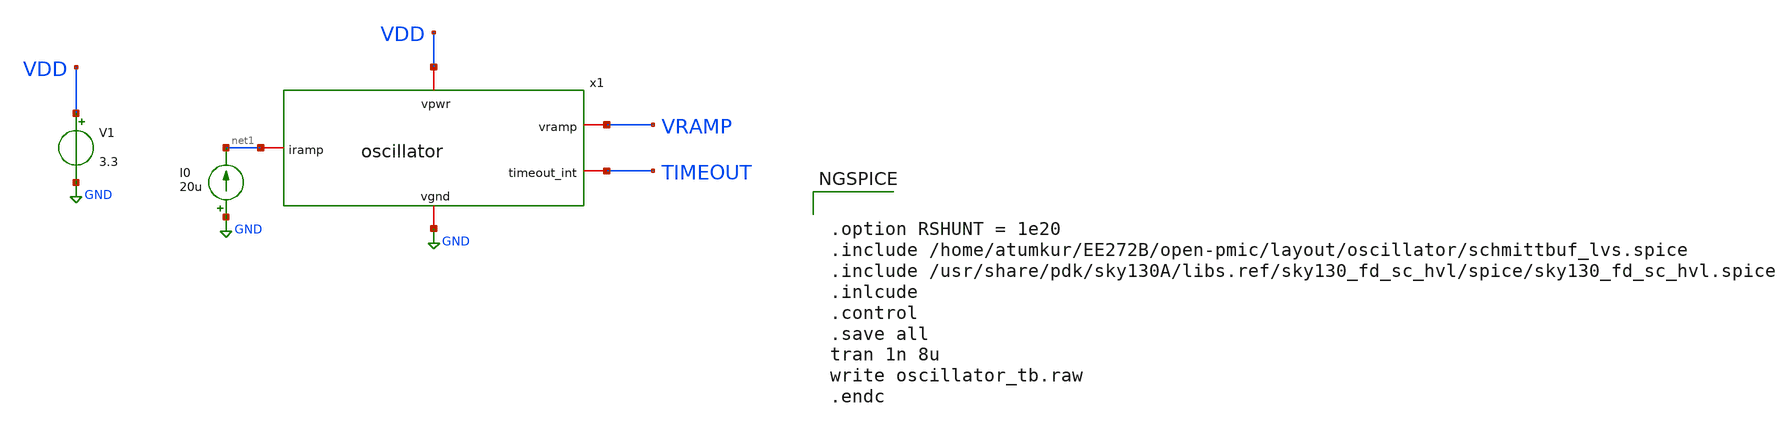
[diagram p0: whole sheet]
** sch_path: design/oscillator/oscillator_tb.sch
**.subckt oscillator_tb
x1 VDD GND net1 VRAMP TIMEOUT oscillator
V1 VDD GND 3.3
I0 GND net1 20u
**** begin user architecture code

.include $::SKYWATER_MODELS/cells/nfet_01v8/sky130_fd_pr__nfet_01v8__tt.corner.spice
.include $::SKYWATER_MODELS/cells/nfet_01v8_lvt/sky130_fd_pr__nfet_01v8_lvt__tt.corner.spice
.include $::SKYWATER_MODELS/cells/pfet_01v8/sky130_fd_pr__pfet_01v8__tt.corner.spice
.include $::SKYWATER_MODELS/cells/nfet_03v3_nvt/sky130_fd_pr__nfet_03v3_nvt__tt.corner.spice
.include $::SKYWATER_MODELS/cells/nfet_05v0_nvt/sky130_fd_pr__nfet_05v0_nvt__tt.corner.spice
.include $::SKYWATER_MODELS/cells/esd_nfet_01v8/sky130_fd_pr__esd_nfet_01v8__tt.corner.spice
.include $::SKYWATER_MODELS/cells/pfet_01v8_lvt/sky130_fd_pr__pfet_01v8_lvt__tt.corner.spice
.include $::SKYWATER_MODELS/cells/pfet_01v8_hvt/sky130_fd_pr__pfet_01v8_hvt__tt.corner.spice
.include $::SKYWATER_MODELS/cells/esd_pfet_g5v0d10v5/sky130_fd_pr__esd_pfet_g5v0d10v5__tt.corner.spice
.include $::SKYWATER_MODELS/cells/pfet_g5v0d10v5/sky130_fd_pr__pfet_g5v0d10v5__tt.corner.spice
.include $::SKYWATER_MODELS/cells/pfet_g5v0d16v0/sky130_fd_pr__pfet_g5v0d16v0__tt.corner.spice
.include $::SKYWATER_MODELS/cells/nfet_g5v0d10v5/sky130_fd_pr__nfet_g5v0d10v5__tt.corner.spice
.include $::SKYWATER_MODELS/cells/nfet_g5v0d16v0/sky130_fd_pr__nfet_g5v0d16v0__tt_discrete.corner.spice
.include $::SKYWATER_MODELS/cells/esd_nfet_g5v0d10v5/sky130_fd_pr__esd_nfet_g5v0d10v5__tt.corner.spice
.include $::SKYWATER_MODELS/models/corners/tt/nonfet.spice
* Mismatch parameters
.include $::SKYWATER_MODELS/cells/nfet_01v8/sky130_fd_pr__nfet_01v8__mismatch.corner.spice
.include $::SKYWATER_MODELS/cells/pfet_01v8/sky130_fd_pr__pfet_01v8__mismatch.corner.spice
.include $::SKYWATER_MODELS/cells/nfet_01v8_lvt/sky130_fd_pr__nfet_01v8_lvt__mismatch.corner.spice
.include $::SKYWATER_MODELS/cells/pfet_01v8_lvt/sky130_fd_pr__pfet_01v8_lvt__mismatch.corner.spice
.include $::SKYWATER_MODELS/cells/pfet_01v8_hvt/sky130_fd_pr__pfet_01v8_hvt__mismatch.corner.spice
.include $::SKYWATER_MODELS/cells/nfet_g5v0d10v5/sky130_fd_pr__nfet_g5v0d10v5__mismatch.corner.spice
.include $::SKYWATER_MODELS/cells/pfet_g5v0d10v5/sky130_fd_pr__pfet_g5v0d10v5__mismatch.corner.spice
.include $::SKYWATER_MODELS/cells/nfet_05v0_nvt/sky130_fd_pr__nfet_05v0_nvt__mismatch.corner.spice
.include $::SKYWATER_MODELS/cells/nfet_03v3_nvt/sky130_fd_pr__nfet_03v3_nvt__mismatch.corner.spice
* Resistor$::SKYWATER_MODELS/Capacitor
.include $::SKYWATER_MODELS/models/r+c/res_typical__cap_typical.spice
.include $::SKYWATER_MODELS/models/r+c/res_typical__cap_typical__lin.spice
* Special cells
.include $::SKYWATER_MODELS/models/corners/tt/specialized_cells.spice
* All models
.include $::SKYWATER_MODELS/models/all.spice
* Corner
.include $::SKYWATER_MODELS/models/corners/tt/rf.spice



.option RSHUNT = 1e20
.include /home/atumkur/EE272B/open-pmic/layout/oscillator/schmittbuf_lvs.spice
.include /usr/share/pdk/sky130A/libs.ref/sky130_fd_sc_hvl/spice/sky130_fd_sc_hvl.spice
.inlcude
.control
.save all
tran 1n 8u
write oscillator_tb.raw
.endc


**** end user architecture code
**.ends

* expanding   symbol:  design/oscillator/oscillator.sym # of pins=5
** sym_path: design/oscillator/oscillator.sym
** sch_path: design/oscillator/oscillator.sch
.subckt oscillator vpwr vgnd iramp vramp timeout_int
*.iopin vpwr
*.iopin vgnd
*.iopin iramp
*.iopin vramp
*.iopin timeout_int
x1 net4 vgnd net5 net6 iramp vramp net2 rampgen
x3 timeout_int VGND VNB VPB VPWR net1 sky130_fd_sc_hvl__inv_1
x4 net1 VGND VNB VPB VPWR net2 sky130_fd_sc_hvl__inv_4
x5 vramp vgnd vgnd vpwr vpwr timeout_int sky130_fd_sc_hvl__schmittbuf_1
x2 net2 VGND VNB VPB VPWR net3 sky130_fd_sc_hvl__inv_8
.ends


* expanding   symbol:  design/oscillator/rampgen.sym # of pins=7
** sym_path: design/oscillator/rampgen.sym
** sch_path: design/oscillator/rampgen.sch
.subckt rampgen VPWR VGND VPB VNB IRAMP VRAMP RAMPGEN_EN
*.iopin VPWR
*.iopin VGND
*.iopin VPB
*.iopin VNB
*.iopin IRAMP
*.iopin VRAMP
*.iopin RAMPGEN_EN
XM1 IRAMP IRAMP VGND VNB sky130_fd_pr__nfet_g5v0d10v5 L=1 W=5 nf=1 ad='int((nf+1)/2) * W/nf * 0.29' as='int((nf+2)/2) * W/nf * 0.29'
+ pd='2*int((nf+1)/2) * (W/nf + 0.29)' ps='2*int((nf+2)/2) * (W/nf + 0.29)' nrd='0.29 / W' nrs='0.29 / W'
+ sa=0 sb=0 sd=0 mult=1 m=1
XM2 net3 IRAMP VGND VNB sky130_fd_pr__nfet_g5v0d10v5 L=1 W=5 nf=1 ad='int((nf+1)/2) * W/nf * 0.29' as='int((nf+2)/2) * W/nf * 0.29'
+ pd='2*int((nf+1)/2) * (W/nf + 0.29)' ps='2*int((nf+2)/2) * (W/nf + 0.29)' nrd='0.29 / W' nrs='0.29 / W'
+ sa=0 sb=0 sd=0 mult=1 m=1
XM3 net2 IRAMP VGND VNB sky130_fd_pr__nfet_g5v0d10v5 L=1 W=5 nf=1 ad='int((nf+1)/2) * W/nf * 0.29' as='int((nf+2)/2) * W/nf * 0.29'
+ pd='2*int((nf+1)/2) * (W/nf + 0.29)' ps='2*int((nf+2)/2) * (W/nf + 0.29)' nrd='0.29 / W' nrs='0.29 / W'
+ sa=0 sb=0 sd=0 mult=15 m=15
XM4 VRAMP RAMPGEN_EN net2 VNB sky130_fd_pr__nfet_g5v0d10v5 L=1 W=5 nf=1 ad='int((nf+1)/2) * W/nf * 0.29'
+ as='int((nf+2)/2) * W/nf * 0.29' pd='2*int((nf+1)/2) * (W/nf + 0.29)' ps='2*int((nf+2)/2) * (W/nf + 0.29)'
+ nrd='0.29 / W' nrs='0.29 / W' sa=0 sb=0 sd=0 mult=15 m=15
XM5 net3 net3 VPWR VPB sky130_fd_pr__pfet_g5v0d10v5 L=1 W=5 nf=1 ad='int((nf+1)/2) * W/nf * 0.29' as='int((nf+2)/2) * W/nf * 0.29'
+ pd='2*int((nf+1)/2) * (W/nf + 0.29)' ps='2*int((nf+2)/2) * (W/nf + 0.29)' nrd='0.29 / W' nrs='0.29 / W'
+ sa=0 sb=0 sd=0 mult=1 m=1
XM6 VRAMP RAMPGEN_EN net1 VPB sky130_fd_pr__pfet_g5v0d10v5 L=1 W=5 nf=1 ad='int((nf+1)/2) * W/nf * 0.29'
+ as='int((nf+2)/2) * W/nf * 0.29' pd='2*int((nf+1)/2) * (W/nf + 0.29)' ps='2*int((nf+2)/2) * (W/nf + 0.29)'
+ nrd='0.29 / W' nrs='0.29 / W' sa=0 sb=0 sd=0 mult=1 m=1
XM7 net1 net3 VPWR VPB sky130_fd_pr__pfet_g5v0d10v5 L=1 W=5 nf=1 ad='int((nf+1)/2) * W/nf * 0.29' as='int((nf+2)/2) * W/nf * 0.29'
+ pd='2*int((nf+1)/2) * (W/nf + 0.29)' ps='2*int((nf+2)/2) * (W/nf + 0.29)' nrd='0.29 / W' nrs='0.29 / W'
+ sa=0 sb=0 sd=0 mult=1 m=1
XC1 VRAMP VGND sky130_fd_pr__cap_mim_m3_1 W=20 L=26 MF=1 m=1
.ends

.GLOBAL GND
**** begin user architecture code
[sky130_models]
**** end user architecture code
.end
